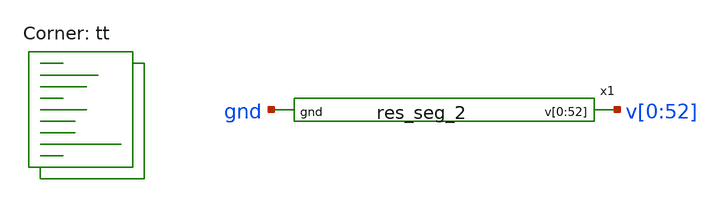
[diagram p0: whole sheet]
** sch_path: xschem/res_seg_2-tb.sch
**.subckt res_seg_2-tb
x1 v[0] v[1] v[2] v[3] v[4] v[5] v[6] v[7] v[8] v[9] v[10] v[11] v[12] v[13] v[14] v[15] v[16] v[17]
+ v[18] v[19] v[20] v[21] v[22] v[23] v[24] v[25] v[26] v[27] v[28] v[29] v[30] v[31] v[32] v[33] v[34]
+ v[35] v[36] v[37] v[38] v[39] v[40] v[41] v[42] v[43] v[44] v[45] v[46] v[47] v[48] v[49] v[50] v[51]
+ v[52] gnd res_seg_2
**** begin user architecture code



  .param max_freq=500e3 period={1/max_freq} time_high={period/2}
  .param delay_vin1={time_high} delay_vin2={time_high*1.5}
  .param lval=100u

  .option wnflag=1
  .option safecurrents

  V52 v[52] gnd dc 3.85
  v0 v[0] gnd dc 0.8741
  *Vin  in  gnd pulse(0 1.8 {delay_vin1} 1p 1p {time_high} {period})
  *Vinb inb gnd pulse(1.8 0 {delay_vin1} 1p 1p {time_high} {period})

  .control
     reset
     save all
     tran 0.1n 100n
     write res_seg_2-tb.raw
     set appendwrite

     *reset
     *save all
     *dc vref 0 1.8 0.1
     *write lvsf-tb.raw
*    quit 0
  .endc



.lib $::SKYWATER_MODELS/sky130.lib.spice tt
**** end user architecture code
**.ends

* expanding   symbol:  res_seg_2.sym # of pins=2
** sym_path: xschem/res_seg_2.sym
** sch_path: xschem/res_seg_2.sch
.subckt res_seg_2 v[0] v[1] v[2] v[3] v[4] v[5] v[6] v[7] v[8] v[9] v[10] v[11] v[12] v[13] v[14]
+ v[15] v[16] v[17] v[18] v[19] v[20] v[21] v[22] v[23] v[24] v[25] v[26] v[27] v[28] v[29] v[30] v[31]
+ v[32] v[33] v[34] v[35] v[36] v[37] v[38] v[39] v[40] v[41] v[42] v[43] v[44] v[45] v[46] v[47] v[48]
+ v[49] v[50] v[51] v[52] gnd
*.opin
*+ v[0],v[1],v[2],v[3],v[4],v[5],v[6],v[7],v[8],v[9],v[10],v[11],v[12],v[13],v[14],v[15],v[16],v[17],v[18],v[19],v[20],v[21],v[22],v[23],v[24],v[25],v[26],v[27],v[28],v[29],v[30],v[31],v[32],v[33],v[34],v[35],v[36],v[37],v[38],v[39],v[40],v[41],v[42],v[43],v[44],v[45],v[46],v[47],v[48],v[49],v[50],v[51],v[52]
*.ipin gnd
XR1 v[1] v[0] gnd sky130_fd_pr__res_xhigh_po_0p35 L=1.9228 mult=1 m=1
XR2 v[2] v[1] gnd sky130_fd_pr__res_xhigh_po_0p35 L=1.7092 mult=1 m=1
XR3 v[3] v[2] gnd sky130_fd_pr__res_xhigh_po_0p35 L=1.5468 mult=1 m=1
XR4 v[4] v[3] gnd sky130_fd_pr__res_xhigh_po_0p35 L=1.4357 mult=1 m=1
XR5 v[5] v[4] gnd sky130_fd_pr__res_xhigh_po_0p35 L=1.3246 mult=1 m=1
XR6 v[6] v[5] gnd sky130_fd_pr__res_xhigh_po_0p35 L=1.2562 mult=1 m=1
XR7 v[7] v[6] gnd sky130_fd_pr__res_xhigh_po_0p35 L=1.1879 mult=1 m=1
XR8 v[8] v[7] gnd sky130_fd_pr__res_xhigh_po_0p35 L=1.128 mult=1 m=1
XR9 v[9] v[8] gnd sky130_fd_pr__res_xhigh_po_0p35 L=1.0853 mult=1 m=1
XR10 v[10] v[9] gnd sky130_fd_pr__res_xhigh_po_0p35 L=1.0511 mult=1 m=1
XR11 v[11] v[10] gnd sky130_fd_pr__res_xhigh_po_0p35 L=1.0084 mult=1 m=1
XR12 v[12] v[11] gnd sky130_fd_pr__res_xhigh_po_0p35 L=0.9828 mult=1 m=1
XR13 v[13] v[12] gnd sky130_fd_pr__res_xhigh_po_0p35 L=0.9571 mult=1 m=1
XR14 v[14] v[13] gnd sky130_fd_pr__res_xhigh_po_0p35 L=0.9315 mult=1 m=1
XR15 v[15] v[14] gnd sky130_fd_pr__res_xhigh_po_0p35 L=0.9059 mult=1 m=1
XR16 v[16] v[15] gnd sky130_fd_pr__res_xhigh_po_0p35 L=0.8973 mult=1 m=1
XR17 v[17] v[16] gnd sky130_fd_pr__res_xhigh_po_0p35 L=0.8802 mult=1 m=1
XR18 v[18] v[17] gnd sky130_fd_pr__res_xhigh_po_0p35 L=0.8631 mult=1 m=1
XR19 v[19] v[18] gnd sky130_fd_pr__res_xhigh_po_0p35 L=0.8546 mult=1 m=1
XR20 v[20] v[19] gnd sky130_fd_pr__res_xhigh_po_0p35 L=0.8375 mult=1 m=1
XR21 v[21] v[20] gnd sky130_fd_pr__res_xhigh_po_0p35 L=0.8375 mult=1 m=1
XR22 v[22] v[21] gnd sky130_fd_pr__res_xhigh_po_0p35 L=0.8289 mult=1 m=1
XR23 v[23] v[22] gnd sky130_fd_pr__res_xhigh_po_0p35 L=0.8204 mult=1 m=1
XR24 v[24] v[23] gnd sky130_fd_pr__res_xhigh_po_0p35 L=0.8118 mult=1 m=1
XR25 v[25] v[24] gnd sky130_fd_pr__res_xhigh_po_0p35 L=0.8118 mult=1 m=1
XR27 v[27] v[26] gnd sky130_fd_pr__res_xhigh_po_0p35 L=0.8033 mult=1 m=1
XR33 v[33] v[32] gnd sky130_fd_pr__res_xhigh_po_0p35 L=0.8204 mult=1 m=1
XR35 v[35] v[34] gnd sky130_fd_pr__res_xhigh_po_0p35 L=0.8289 mult=1 m=1
XR36 v[36] v[35] gnd sky130_fd_pr__res_xhigh_po_0p35 L=0.8460 mult=1 m=1
XR38 v[38] v[37] gnd sky130_fd_pr__res_xhigh_po_0p35 L=0.8631 mult=1 m=1
XR39 v[39] v[38] gnd sky130_fd_pr__res_xhigh_po_0p35 L=0.8717 mult=1 m=1
XR40 v[40] v[39] gnd sky130_fd_pr__res_xhigh_po_0p35 L=0.8802 mult=1 m=1
XR41 v[41] v[40] gnd sky130_fd_pr__res_xhigh_po_0p35 L=0.9059 mult=1 m=1
XR42 v[42] v[41] gnd sky130_fd_pr__res_xhigh_po_0p35 L=0.9144 mult=1 m=1
XR43 v[43] v[42] gnd sky130_fd_pr__res_xhigh_po_0p35 L=0.94 mult=1 m=1
XR44 v[44] v[43] gnd sky130_fd_pr__res_xhigh_po_0p35 L=0.9657 mult=1 m=1
XR45 v[45] v[44] gnd sky130_fd_pr__res_xhigh_po_0p35 L=0.9913 mult=1 m=1
XR46 v[46] v[45] gnd sky130_fd_pr__res_xhigh_po_0p35 L=1.0169 mult=1 m=1
XR47 v[47] v[46] gnd sky130_fd_pr__res_xhigh_po_0p35 L=1.0511 mult=1 m=1
XR48 v[48] v[47] gnd sky130_fd_pr__res_xhigh_po_0p35 L=1.0853 mult=1 m=1
XR49 v[49] v[48] gnd sky130_fd_pr__res_xhigh_po_0p35 L=1.1366 mult=1 m=1
XR50 v[50] v[49] gnd sky130_fd_pr__res_xhigh_po_0p35 L=1.1879 mult=1 m=1
XR51 v[51] v[50] gnd sky130_fd_pr__res_xhigh_po_0p35 L=1.2477 mult=1 m=1
XR52 v[52] v[51] gnd sky130_fd_pr__res_xhigh_po_0p35 L=1.316 mult=1 m=1
XR26 v[26] v[25] gnd sky130_fd_pr__res_xhigh_po_0p35 L=0.8118 mult=1 m=1
XR28 v[28] v[27] gnd sky130_fd_pr__res_xhigh_po_0p35 L=0.8118 mult=1 m=1
XR29 v[29] v[28] gnd sky130_fd_pr__res_xhigh_po_0p35 L=0.8033 mult=1 m=1
XR30 v[30] v[29] gnd sky130_fd_pr__res_xhigh_po_0p35 L=0.8118 mult=1 m=1
XR31 v[31] v[30] gnd sky130_fd_pr__res_xhigh_po_0p35 L=0.8118 mult=1 m=1
XR32 v[32] v[31] gnd sky130_fd_pr__res_xhigh_po_0p35 L=0.8118 mult=1 m=1
XR34 v[34] v[33] gnd sky130_fd_pr__res_xhigh_po_0p35 L=0.8204 mult=1 m=1
XR37 v[37] v[36] gnd sky130_fd_pr__res_xhigh_po_0p35 L=0.8460 mult=1 m=1
.ends

.end
